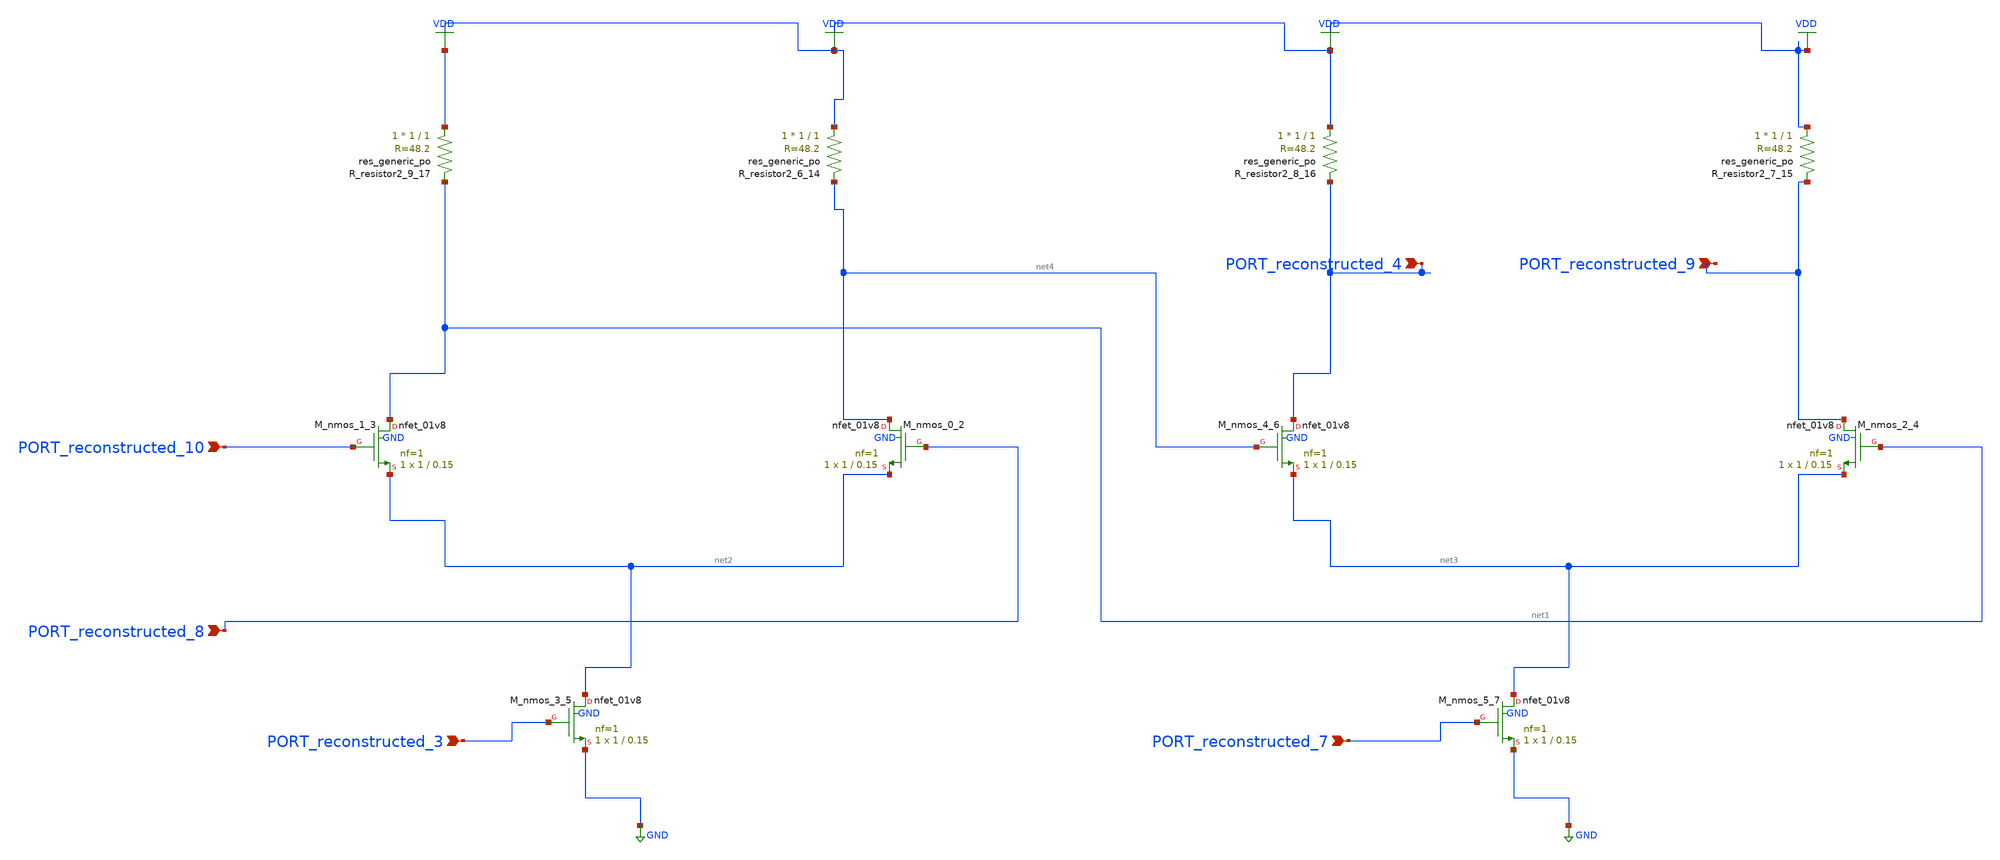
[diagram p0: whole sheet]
** sch_path: schematics/AMSNet/320.sch
**.subckt 320 PORT_reconstructed_8 PORT_reconstructed_4 PORT_reconstructed_9 PORT_reconstructed_10
*+ PORT_reconstructed_3 PORT_reconstructed_7
*.ipin PORT_reconstructed_8
*.ipin PORT_reconstructed_4
*.ipin PORT_reconstructed_9
*.ipin PORT_reconstructed_10
*.ipin PORT_reconstructed_3
*.ipin PORT_reconstructed_7
XM_nmos_0_2 net4 PORT_reconstructed_8 net2 GND sky130_fd_pr__nfet_01v8 L=0.15 W=1 nf=1 ad='int((1 + 1)/2) * 1 / 1 * 0.29'
+ as='int((1 + 2)/2) * 1 / 1 * 0.29' pd='2*int((1 + 1)/2) * (1 / 1 + 0.29)' ps='2*int((1 + 2)/2) * (1 / 1 + 0.29)'
+ nrd='0.29 / 1 ' nrs='0.29 / 1 ' sa=0 sb=0 sd=0 mult=1 m=1
XM_nmos_1_3 net1 PORT_reconstructed_10 net2 GND sky130_fd_pr__nfet_01v8 L=0.15 W=1 nf=1 ad='int((1 + 1)/2) * 1 / 1 * 0.29'
+ as='int((1 + 2)/2) * 1 / 1 * 0.29' pd='2*int((1 + 1)/2) * (1 / 1 + 0.29)' ps='2*int((1 + 2)/2) * (1 / 1 + 0.29)'
+ nrd='0.29 / 1 ' nrs='0.29 / 1 ' sa=0 sb=0 sd=0 mult=1 m=1
XM_nmos_2_4 PORT_reconstructed_9 net1 net3 GND sky130_fd_pr__nfet_01v8 L=0.15 W=1 nf=1 ad='int((1 + 1)/2) * 1 / 1 * 0.29'
+ as='int((1 + 2)/2) * 1 / 1 * 0.29' pd='2*int((1 + 1)/2) * (1 / 1 + 0.29)' ps='2*int((1 + 2)/2) * (1 / 1 + 0.29)'
+ nrd='0.29 / 1 ' nrs='0.29 / 1 ' sa=0 sb=0 sd=0 mult=1 m=1
XM_nmos_3_5 net2 PORT_reconstructed_3 GND GND sky130_fd_pr__nfet_01v8 L=0.15 W=1 nf=1 ad='int((1 + 1)/2) * 1 / 1 * 0.29'
+ as='int((1 + 2)/2) * 1 / 1 * 0.29' pd='2*int((1 + 1)/2) * (1 / 1 + 0.29)' ps='2*int((1 + 2)/2) * (1 / 1 + 0.29)'
+ nrd='0.29 / 1 ' nrs='0.29 / 1 ' sa=0 sb=0 sd=0 mult=1 m=1
XM_nmos_4_6 PORT_reconstructed_4 net4 net3 GND sky130_fd_pr__nfet_01v8 L=0.15 W=1 nf=1 ad='int((1 + 1)/2) * 1 / 1 * 0.29'
+ as='int((1 + 2)/2) * 1 / 1 * 0.29' pd='2*int((1 + 1)/2) * (1 / 1 + 0.29)' ps='2*int((1 + 2)/2) * (1 / 1 + 0.29)'
+ nrd='0.29 / 1 ' nrs='0.29 / 1 ' sa=0 sb=0 sd=0 mult=1 m=1
XM_nmos_5_7 net3 PORT_reconstructed_7 GND GND sky130_fd_pr__nfet_01v8 L=0.15 W=1 nf=1 ad='int((1 + 1)/2) * 1 / 1 * 0.29'
+ as='int((1 + 2)/2) * 1 / 1 * 0.29' pd='2*int((1 + 1)/2) * (1 / 1 + 0.29)' ps='2*int((1 + 2)/2) * (1 / 1 + 0.29)'
+ nrd='0.29 / 1 ' nrs='0.29 / 1 ' sa=0 sb=0 sd=0 mult=1 m=1
XR_resistor2_6_14 VDD net4 sky130_fd_pr__res_generic_po W=1 L=1 m=1
XR_resistor2_7_15 VDD PORT_reconstructed_9 sky130_fd_pr__res_generic_po W=1 L=1 m=1
XR_resistor2_8_16 VDD PORT_reconstructed_4 sky130_fd_pr__res_generic_po W=1 L=1 m=1
XR_resistor2_9_17 VDD net1 sky130_fd_pr__res_generic_po W=1 L=1 m=1
**.ends
.GLOBAL GND
.GLOBAL VDD
.end
